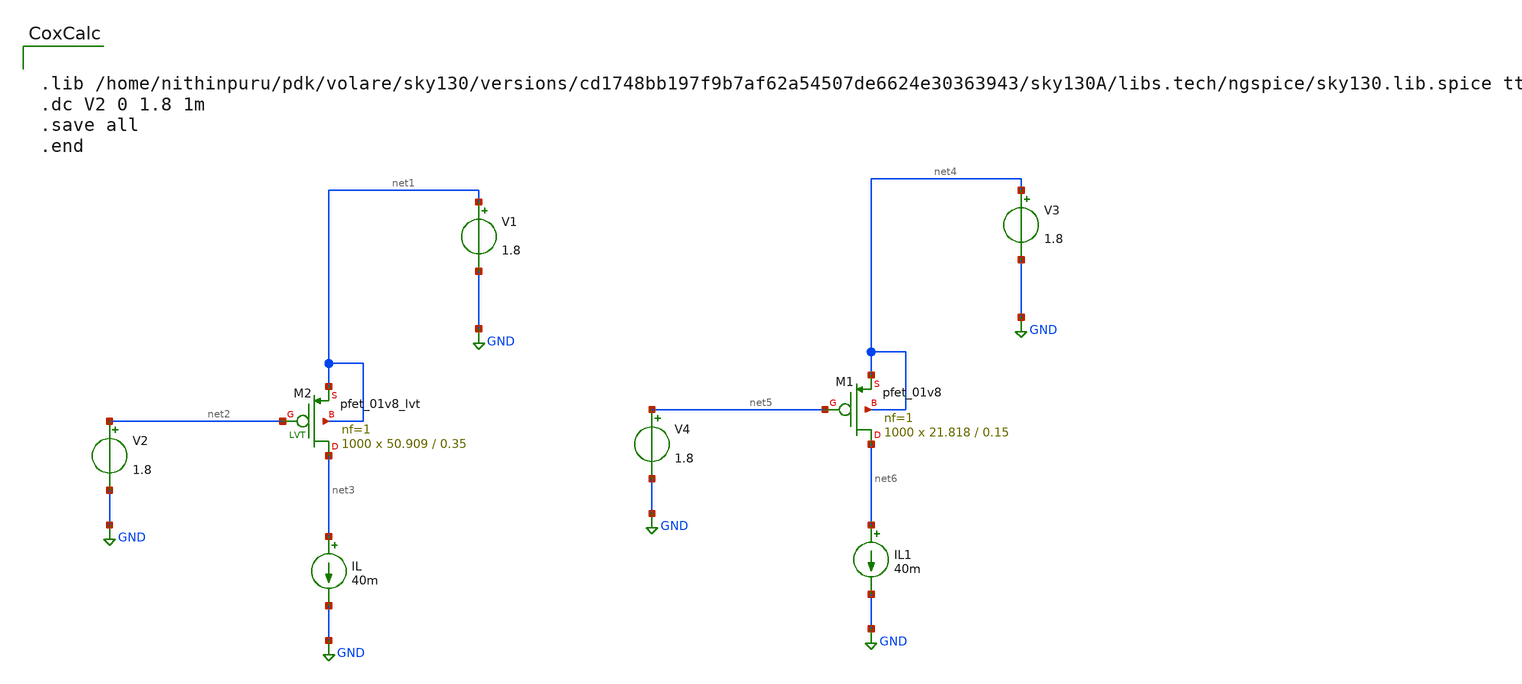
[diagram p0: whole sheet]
** sch_path: Schematics/pass_tran_test.sch
**.subckt pass_tran_test
IL net3 GND 40m
V1 net1 GND 1.8
V2 net2 GND 1.8
XM2 net3 net2 net1 net1 sky130_fd_pr__pfet_01v8_lvt L=0.35 W=50.909 nf=1 ad='int((nf+1)/2) * W/nf * 0.29'
+ as='int((nf+2)/2) * W/nf * 0.29' pd='2*int((nf+1)/2) * (W/nf + 0.29)' ps='2*int((nf+2)/2) * (W/nf + 0.29)'
+ nrd='0.29 / W' nrs='0.29 / W' sa=0 sb=0 sd=0 mult=1000 m=1000
IL1 net6 GND 40m
V3 net4 GND 1.8
V4 net5 GND 1.8
XM1 net6 net5 net4 net4 sky130_fd_pr__pfet_01v8 L=0.15 W=21.818 nf=1 ad='int((nf+1)/2) * W/nf * 0.29'
+ as='int((nf+2)/2) * W/nf * 0.29' pd='2*int((nf+1)/2) * (W/nf + 0.29)' ps='2*int((nf+2)/2) * (W/nf + 0.29)'
+ nrd='0.29 / W' nrs='0.29 / W' sa=0 sb=0 sd=0 mult=1000 m=1000
**** begin user architecture code


.lib /home/nithinpuru/pdk/volare/sky130/versions/cd1748bb197f9b7af62a54507de6624e30363943/sky130A/libs.tech/ngspice/sky130.lib.spice tt
.dc V2 0 1.8 1m
.save all
.end

**** end user architecture code
**.ends
.GLOBAL GND
.end
